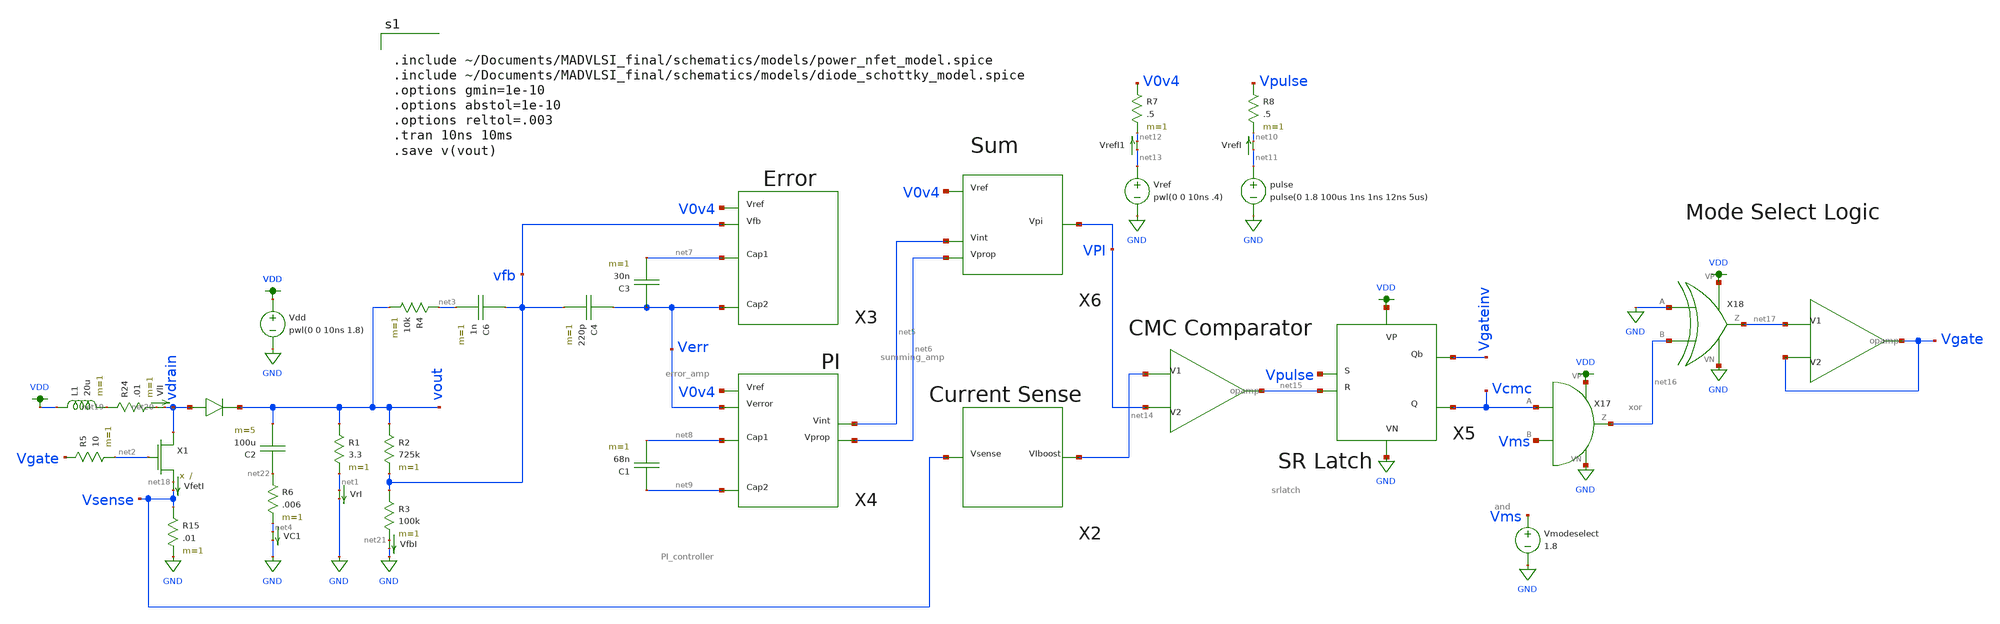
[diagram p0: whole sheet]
** sch_path: schematics/boost_controller_CMC.sch
**.subckt boost_controller_CMC
VfetI net18 Vsense 0
.save i(vfeti)
X1 vdrain net2 net18 power_nfet
L1 VDD net19 20u m=1
D1 vdrain vout diode_schottky
R1 vout net1 3.3 m=1
VlI net20 vdrain 0
.save i(vli)
VrI net1 GND 0
.save i(vri)
R2 vout vfb 725k m=1
R3 vfb net21 100k m=1
Vdd VDD GND pwl(0 0 10ns 1.8)
Vref net13 GND pwl(0 0 10ns .4)
X11 net14 VPI net15 opamp
R24 net19 net20 .01 m=1
VfbI net21 GND 0
.save i(vfbi)
C3 Verr net7 30n m=1
C4 Verr vfb 220p m=1
R4 net3 vout 10k m=1
C6 vfb net3 1n m=1
R5 Vgate net2 10 m=1
C2 net22 vout 100u m=5
R6 net22 net4 .006 m=1
VC1 net4 GND 0
.save i(vc1)
R15 Vsense GND .01 m=1
X5 Vpulse net15 VDD GND Vgateinv Vcmc srlatch
X10 net17 Vgate Vgate opamp
X2 Vsense net14 current_boost
X3 V0v4 net7 vfb Verr error_amp
X4 V0v4 net8 Verr net9 net5 net6 PI_controller
C1 net9 net8 68n m=1
X6 V0v4 VPI net5 net6 summing_amp
Vmodeselect Vms GND 1.8
pulse net11 GND pulse(0 1.8 100us 1ns 1ns 12ns 5us)
VrefI net11 net10 0
.save i(vrefi)
R8 Vpulse net10 .5 m=1
VrefI1 net13 net12 0
.save i(vrefi1)
R7 V0v4 net12 .5 m=1
X17 Vcmc Vms VDD GND net16 and
X18 GND net16 VDD GND net17 xor
**** begin user architecture code


.include ~/Documents/MADVLSI_final/schematics/models/power_nfet_model.spice
.include ~/Documents/MADVLSI_final/schematics/models/diode_schottky_model.spice
.options gmin=1e-10
.options abstol=1e-10
.options reltol=.003
.tran 10ns 10ms
.save v(vout)


.option wnflag=1
.lib ~/skywater/skywater-pdk/libraries/sky130_fd_pr_ngspice/latest/models/sky130.lib.spice tt

**** end user architecture code
**.ends
.GLOBAL GND
.GLOBAL VDD
.end
